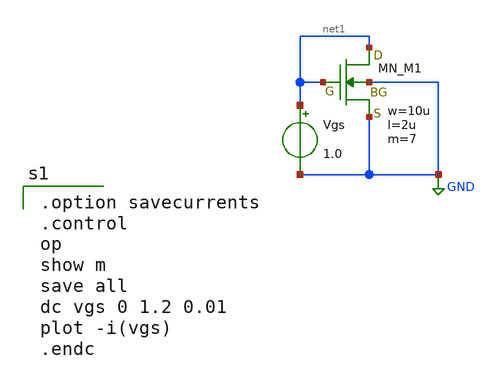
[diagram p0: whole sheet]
** sch_path: member_project/DCDC/xschem/nmos_id_diode.sch
**.subckt nmos_id_diode
Vgs net1 GND 1.0
XM1 net1 net1 GND GND NMOS w=10u l=2u as=0 ad=0 ps=0 pd=0 nrd=0 nrs=0 m=7
**** begin user architecture code
 .include $::LIB/ip62_models

.option savecurrents
.control
op
show m
save all
dc vgs 0 1.2 0.01
plot -i(vgs)
.endc

**** end user architecture code
**.ends
.GLOBAL GND
.end
